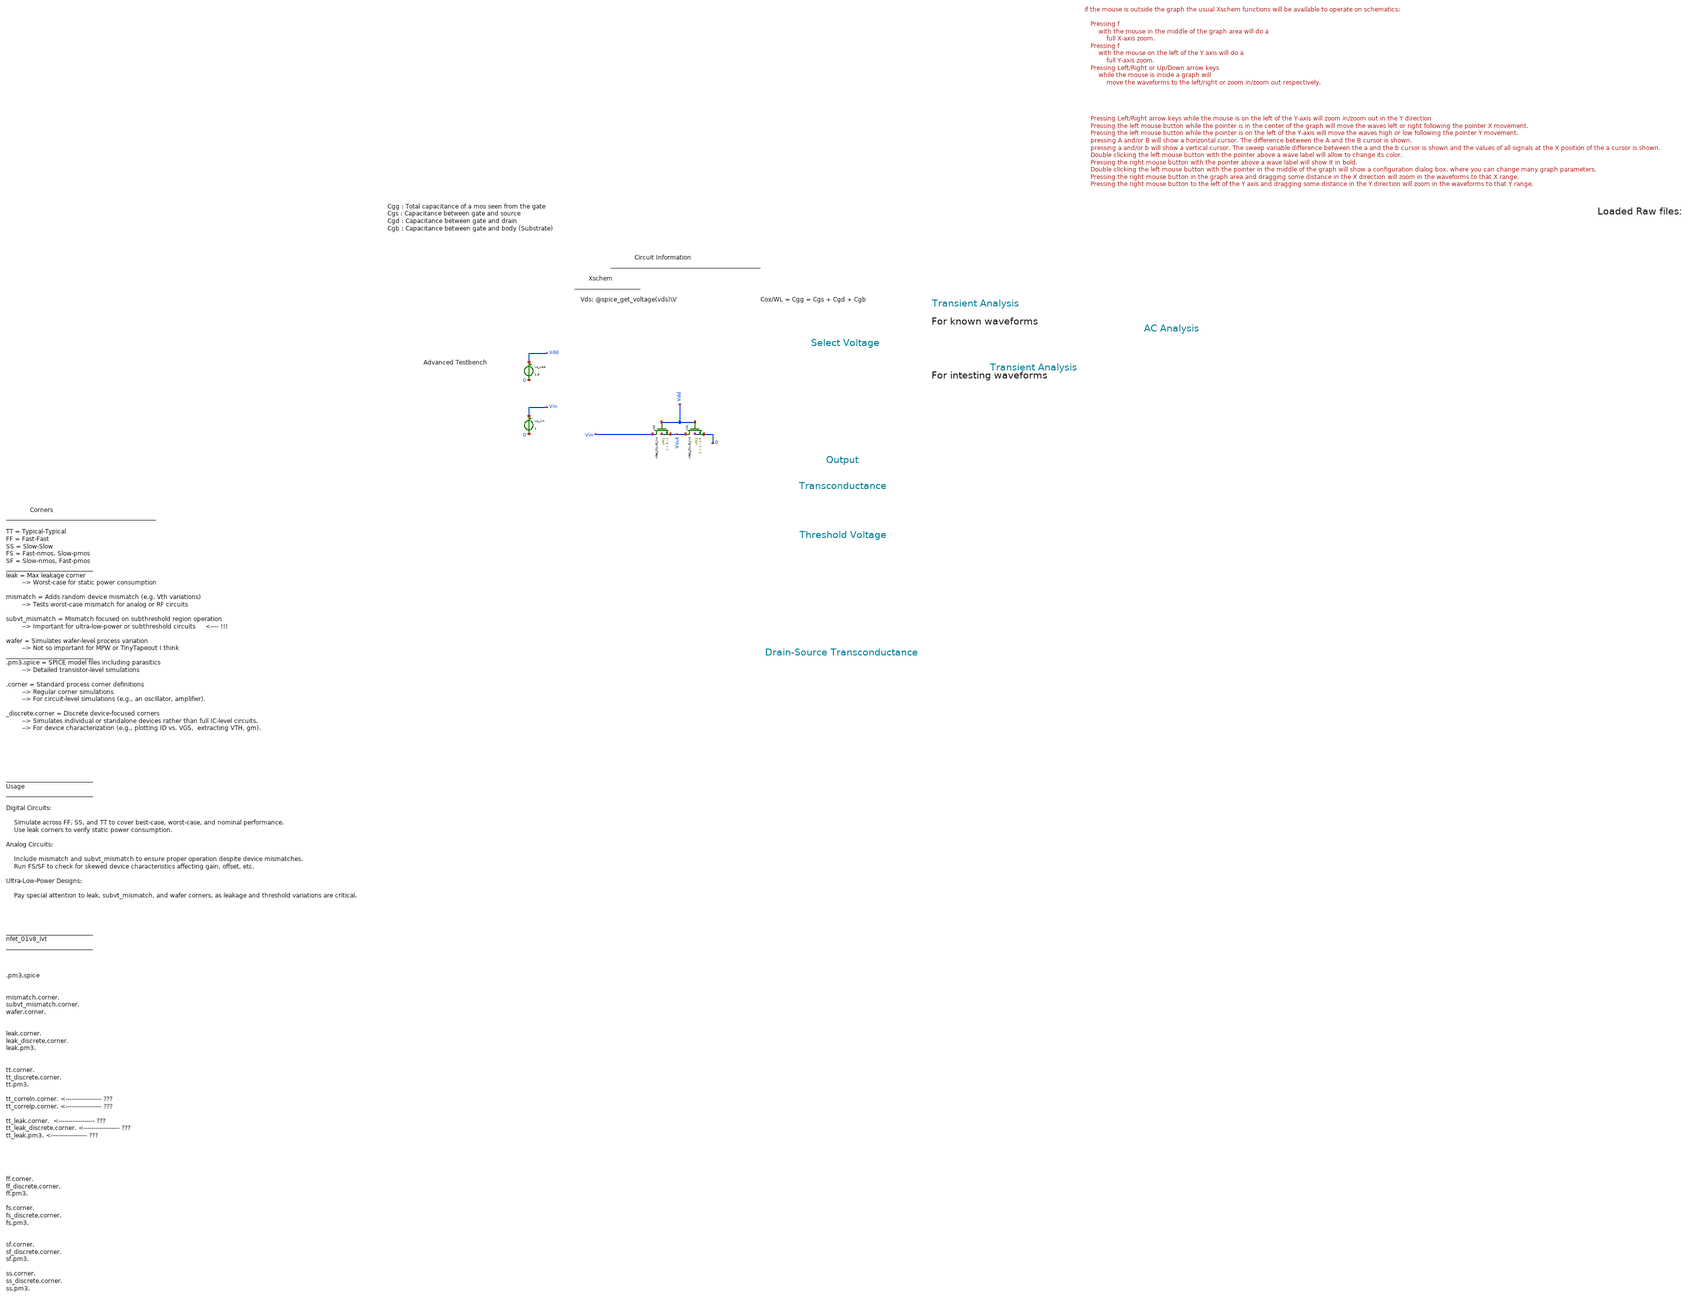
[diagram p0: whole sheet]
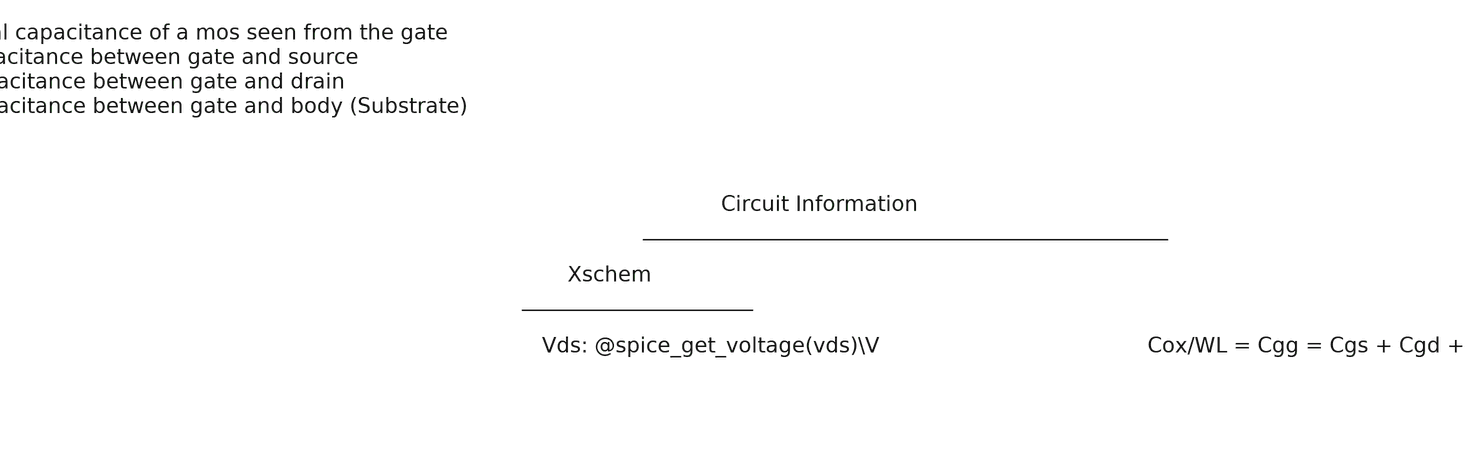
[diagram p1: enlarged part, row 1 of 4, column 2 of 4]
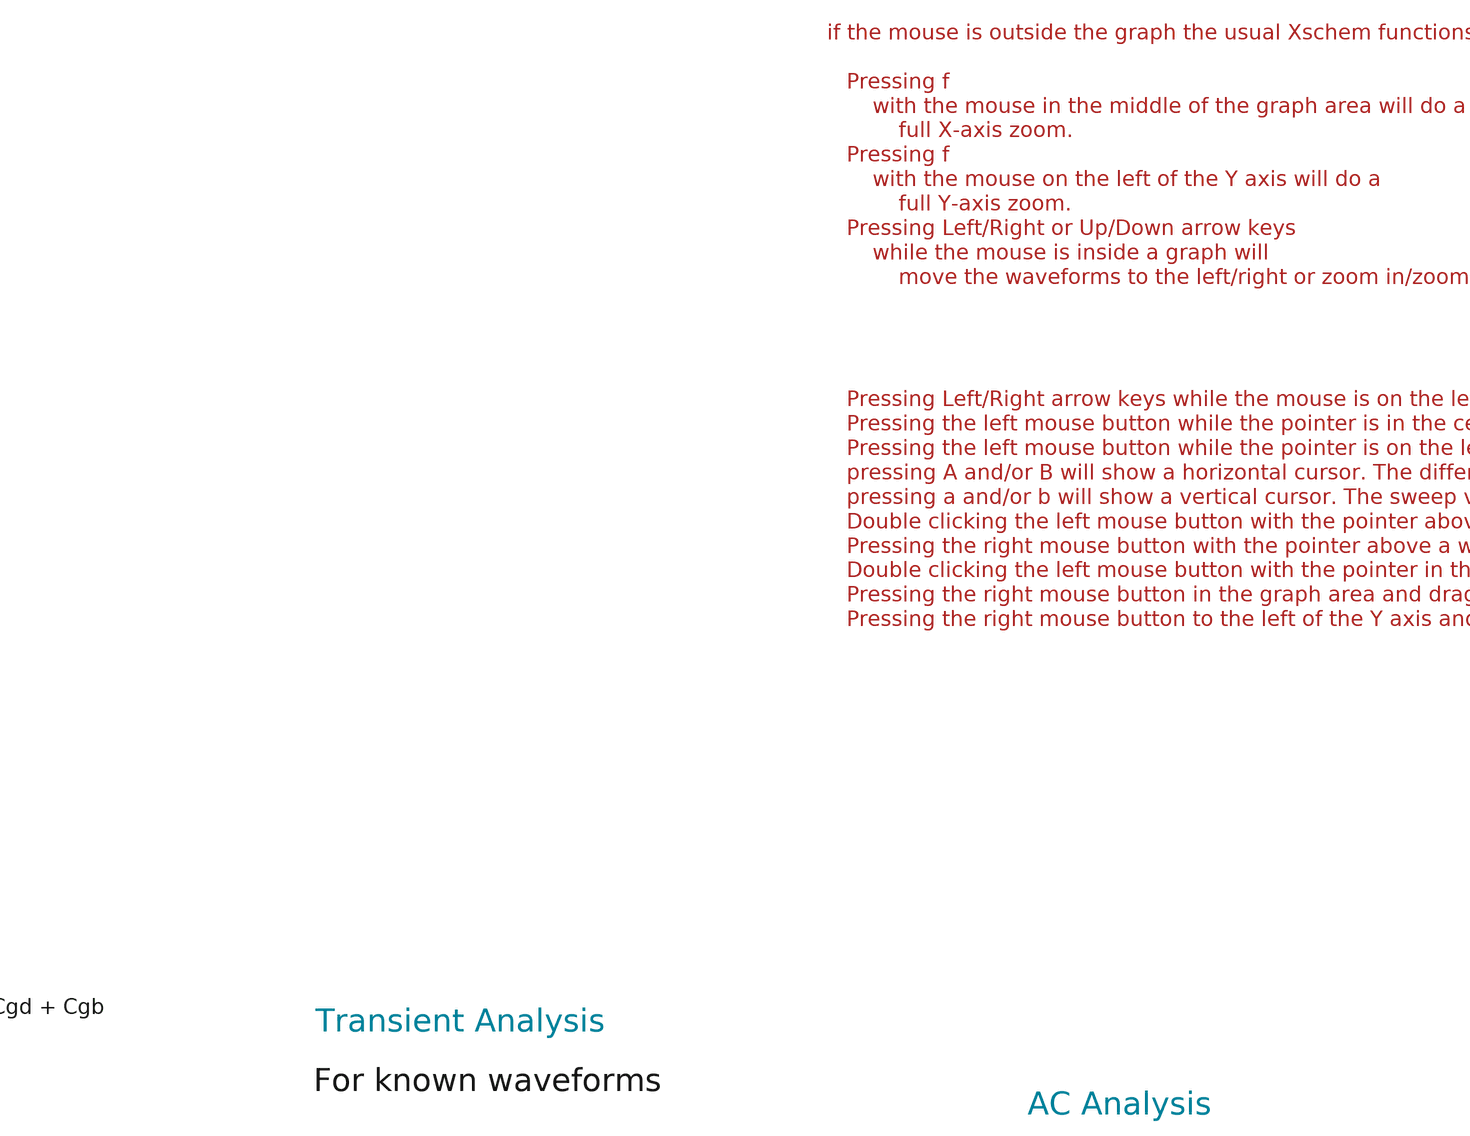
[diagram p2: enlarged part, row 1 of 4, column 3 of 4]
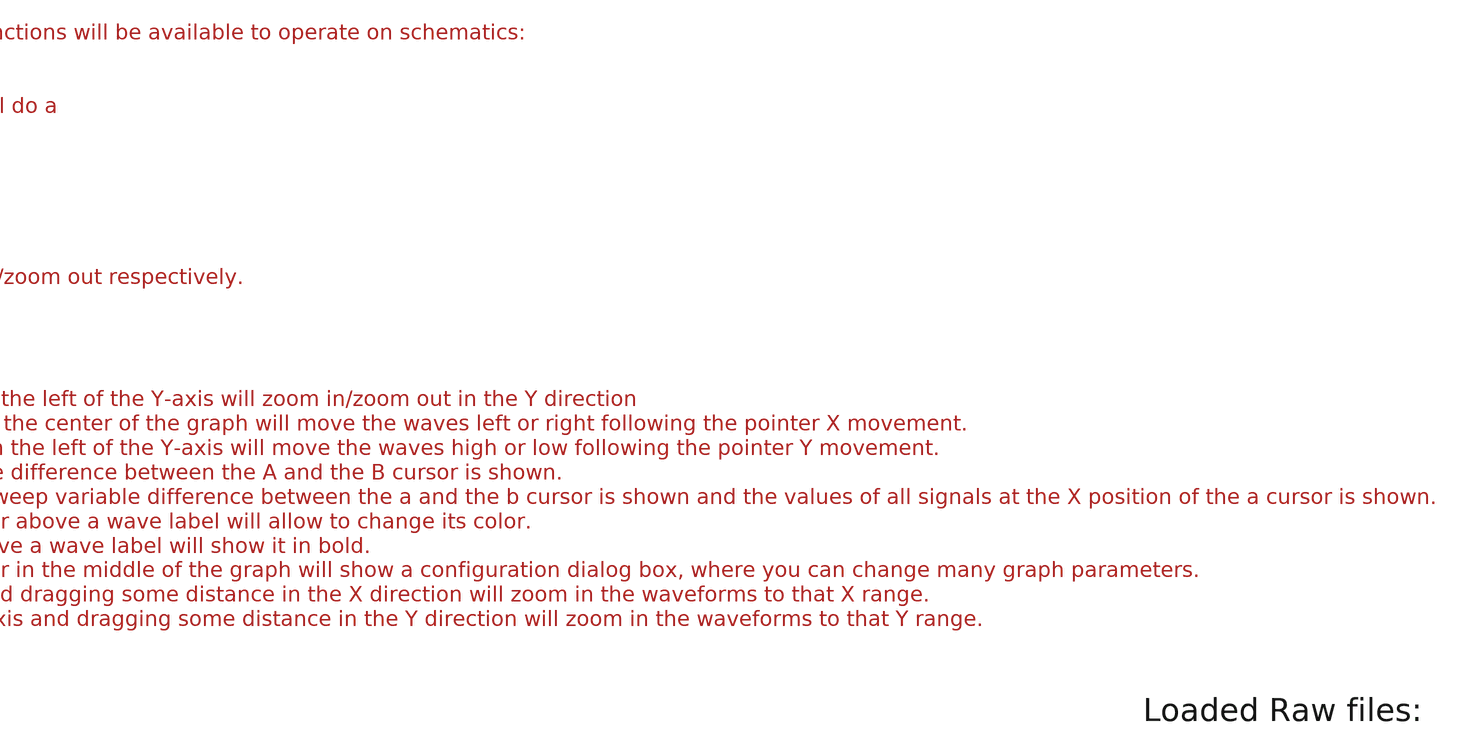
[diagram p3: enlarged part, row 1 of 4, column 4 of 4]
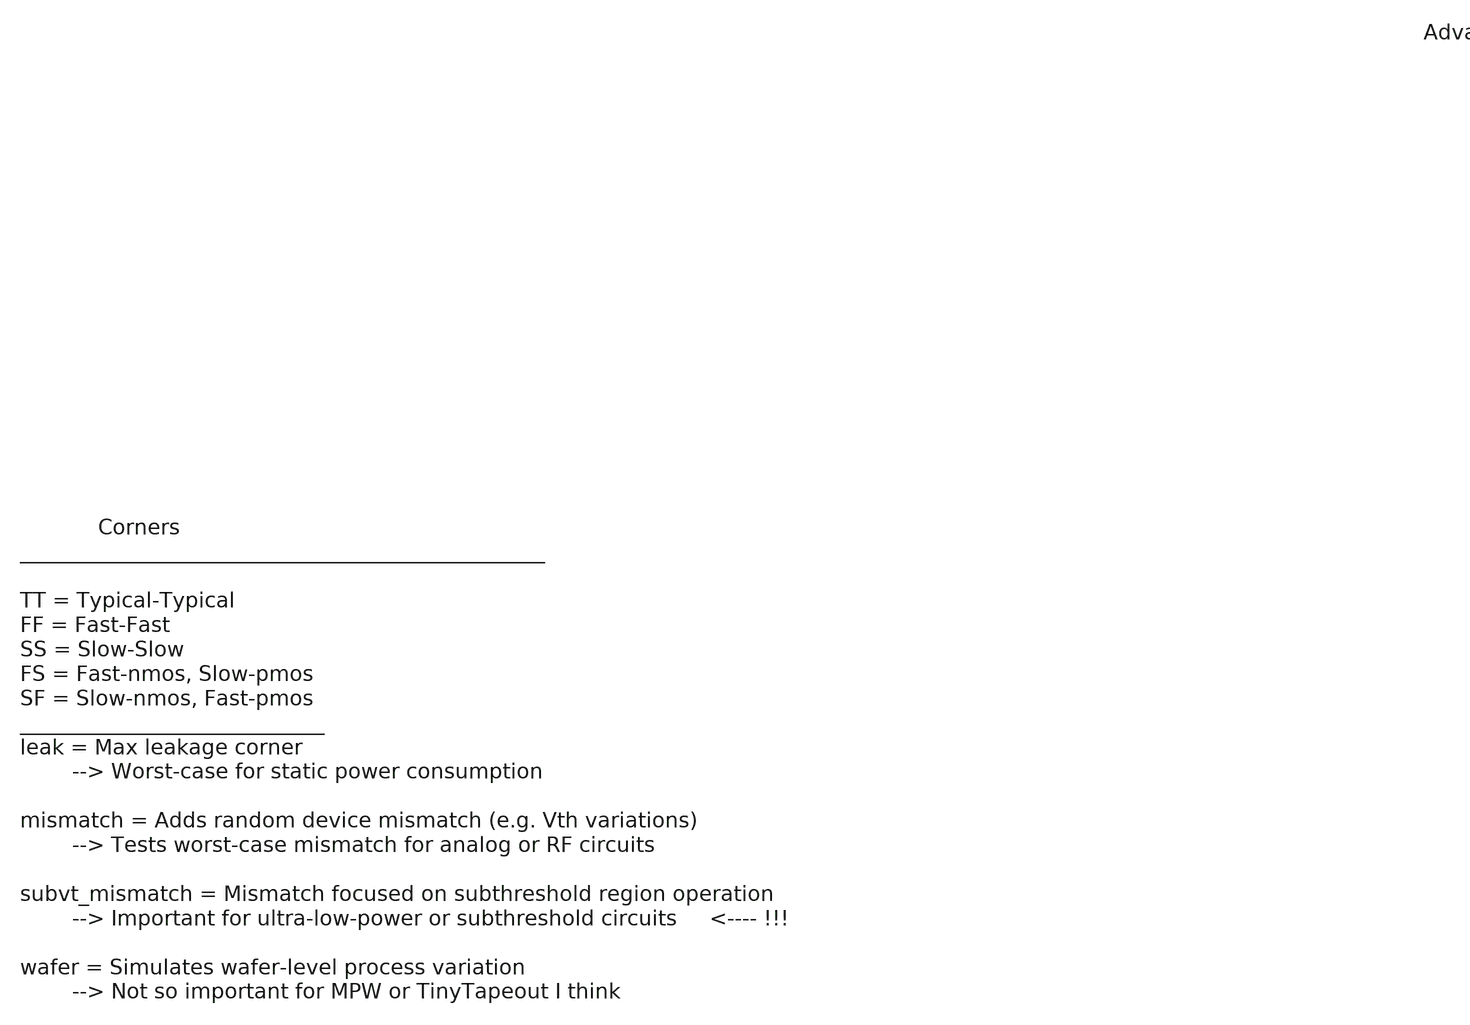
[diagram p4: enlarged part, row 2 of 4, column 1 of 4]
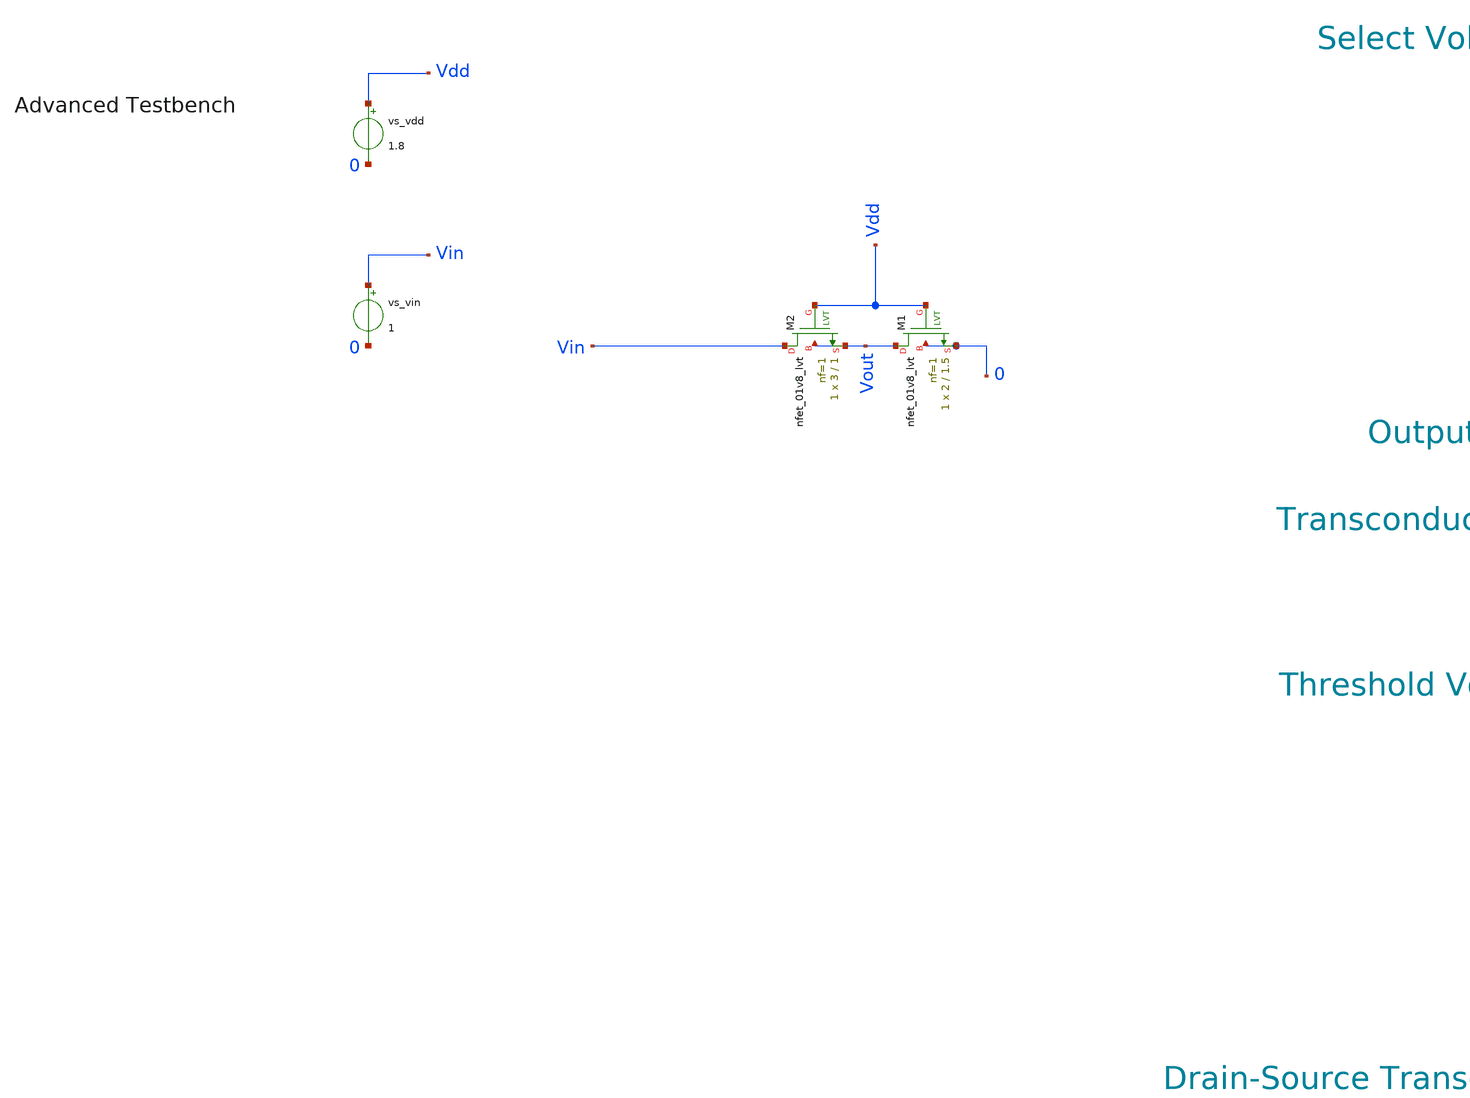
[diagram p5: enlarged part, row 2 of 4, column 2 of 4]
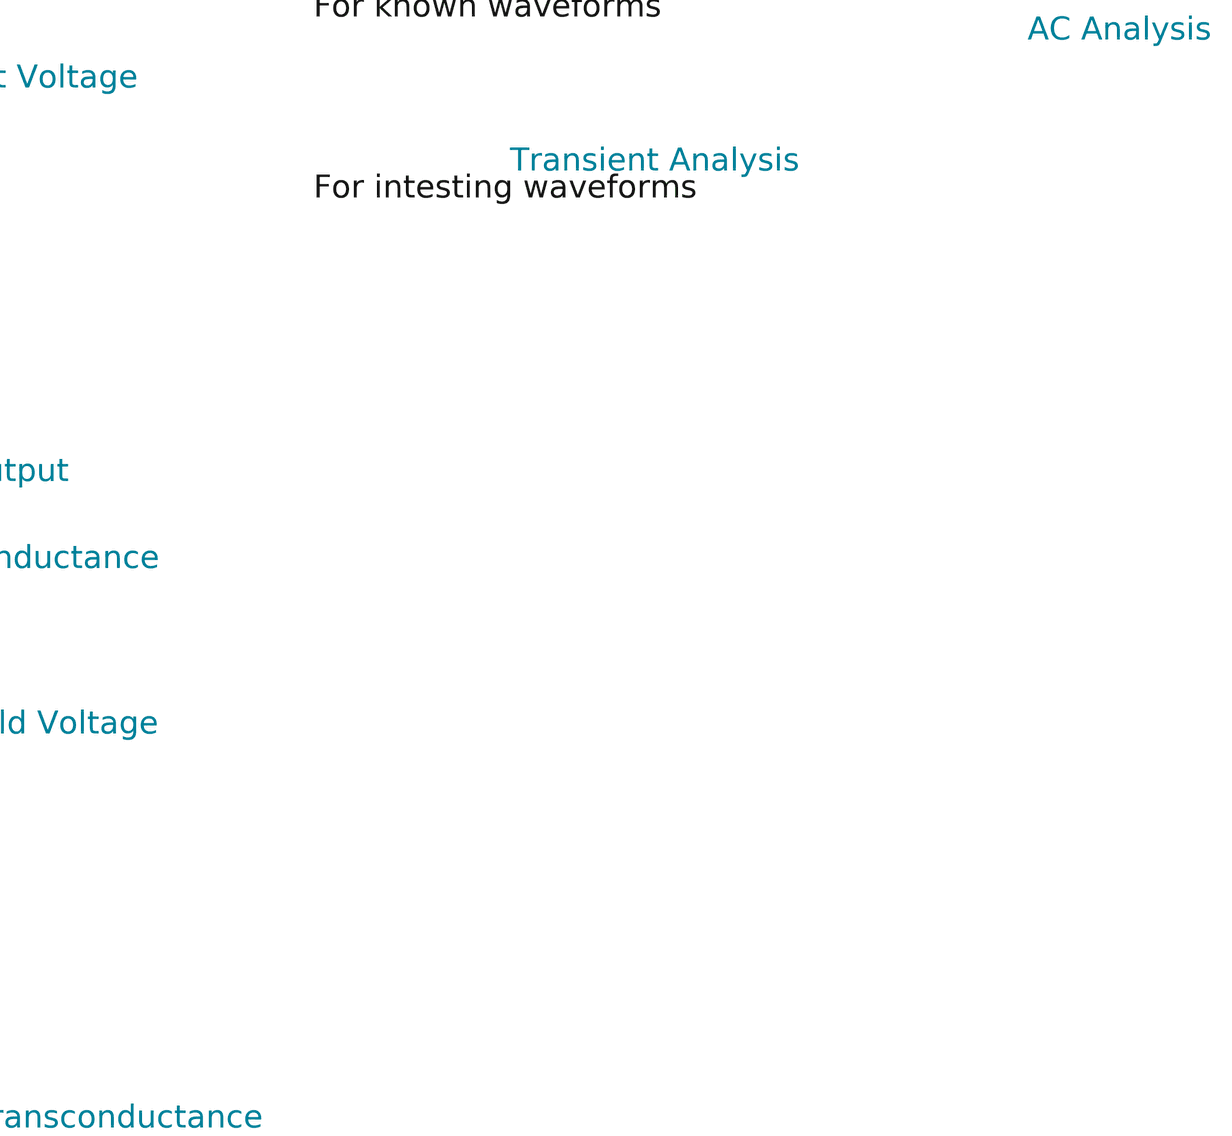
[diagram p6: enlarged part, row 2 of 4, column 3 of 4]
** sch_path: tt10-hdl/tt_um_test_commit/xschem/T0/vPartitioner/voltage_divider_tb.sch
* Copyright (C) 1998-2024 Stefan Frederik Schippers
* This program is free software; you can redistribute it and/or modify
* it under the terms of the GNU General Public License as published by
* the Free Software Foundation; either version 2 of the License, or
* (at your option) any later version.
* This program is distributed in the hope that it will be useful,
* but WITHOUT ANY WARRANTY; without even the implied warranty of
* MERCHANTABILITY or FITNESS FOR A PARTICULAR PURPOSE.  See the
* GNU General Public License for more details.
* You should have received a copy of the GNU General Public License
* along with this program; if not, write to the Free Software
**.subckt voltage_divider_tb
vs_vin Vin 0 1
XM2 Vin Vdd Vout Vout sky130_fd_pr__nfet_01v8_lvt L=1 W=3 nf=1 ad='int((1 + 1)/2) * 3 / 1 * 0.29' as='int((1 + 2)/2) * 3 / 1 * 0.29'
+ pd='2*int((1 + 1)/2) * (3 / 1 + 0.29)' ps='2*int((1 + 2)/2) * (3 / 1 + 0.29)' nrd='0.29 / 3 ' nrs='0.29 / 3 '
+ sa=0 sb=0 sd=0 mult=1 m=1
XM1 Vout Vdd 0 0 sky130_fd_pr__nfet_01v8_lvt L=1.5 W=2 nf=1 ad='int((1 + 1)/2) * 2 / 1 * 0.29' as='int((1 + 2)/2) * 2 / 1 * 0.29'
+ pd='2*int((1 + 1)/2) * (2 / 1 + 0.29)' ps='2*int((1 + 2)/2) * (2 / 1 + 0.29)' nrd='0.29 / 2 ' nrs='0.29 / 2 '
+ sa=0 sb=0 sd=0 mult=1 m=1
vs_vdd Vdd 0 1.8
**** begin user architecture code



.temp 30
*.param w_width = 1
*.param l_length = 0.15
*.option gmin=5n
*.option scale=1e-6
*.option wnflag=1
.option savecurrents

.save all
.control
  save all alli

  save @m.xm1.msky130_fd_pr__nfet_01v8_lvt[gm]
  save @m.xm1.msky130_fd_pr__nfet_01v8_lvt[id]
  save @m.xm1.msky130_fd_pr__nfet_01v8_lvt[vgs]

  save @m.xm1.msky130_fd_pr__nfet_01v8_lvt[cgg]
  save @m.xm1.msky130_fd_pr__nfet_01v8_lvt[cgs]
  save @m.xm1.msky130_fd_pr__nfet_01v8_lvt[cgd]
  save @m.xm1.msky130_fd_pr__nfet_01v8_lvt[cgb]

  save @m.xm1.msky130_fd_pr__nfet_01v8_lvt[vds]
  save @m.xm1.msky130_fd_pr__nfet_01v8_lvt[vdsat]
  save @m.xm1.msky130_fd_pr__nfet_01v8_lvt[vth]


  save @m.xm1.msky130_fd_pr__nfet_01v8_lvt[leff]
  save @m.xm1.msky130_fd_pr__nfet_01v8_lvt[weff]
  save @m.xm1.msky130_fd_pr__nfet_01v8_lvt[gds]
  save @m.xm1.msky130_fd_pr__nfet_01v8_lvt[l]
  save @m.xm1.msky130_fd_pr__nfet_01v8_lvt[w]
  save @m.xm1.msky130_fd_pr__nfet_01v8_lvt[gm]
  save @m.xm1.msky130_fd_pr__nfet_01v8_lvt[gm]
  save @m.xm1.msky130_fd_pr__nfet_01v8_lvt[gm]
  save @m.xm1.msky130_fd_pr__nfet_01v8_lvt[gm]
  save @m.xm1.msky130_fd_pr__nfet_01v8_lvt[gm]


  dc vs_vin 0 1.8  0.005
  *dc v_dev_vds 0 20u  10n
  write nmos_tb.raw


  op
  set appendwrite
  write nmos_tb.raw



  *tran 1n 5u
  *write nmos_tb.raw






  *quit 0




.endc





** opencircuitdesign pdks install
.lib $::SKYWATER_MODELS/sky130.lib.spice tt
.include $::SKYWATER_STDCELLS/sky130_fd_sc_hd.spice


**** end user architecture code
**.ends
.end
